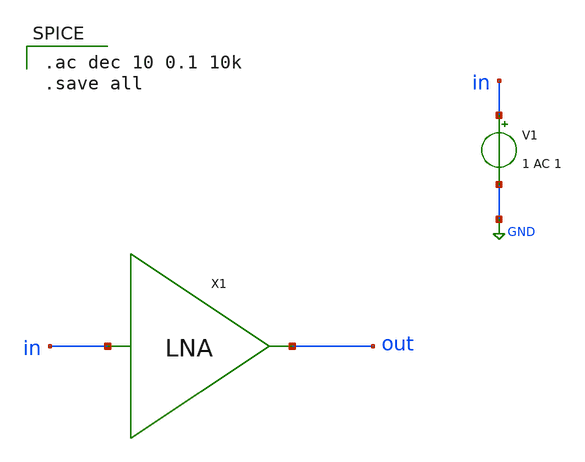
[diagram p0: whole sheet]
** sch_path: xschem/LNA/ideal_lna_TB.sch
**.subckt ideal_lna_TB
X1 in out ideal_lna
V1 in GND 1 AC 1
**** begin user architecture code

.ac dec 10 0.1 10k
.save all

**** end user architecture code
**.ends

* expanding   symbol:  ideal_lna.sym # of pins=2
** sym_path: xschem/LNA/ideal_lna.sym
** sch_path: xschem/LNA/ideal_lna.sch
.subckt ideal_lna vin vout
*.ipin vin
*.opin vout
R1 net3 net1 1k m=1
C1 net3 GND 796n m=1
C2 net2 net4 3.18u m=1
R2 net4 GND 10k m=1
R3 net5 GND 1k m=1
R4 vout net5 99k m=1
X1 vin net1 net1 opamp
X2 net3 net2 net2 opamp
X3 net4 net5 vout opamp
.ends


* expanding   symbol:  MISC/opamp.sym # of pins=3
** sym_path: xschem/MISC/opamp.sym
** sch_path: xschem/MISC/opamp.sch
.subckt opamp vp vm out
*.ipin vp
*.ipin vm
*.opin out
E1 out GND vp vm 1E6
.ends

.GLOBAL GND
.end
